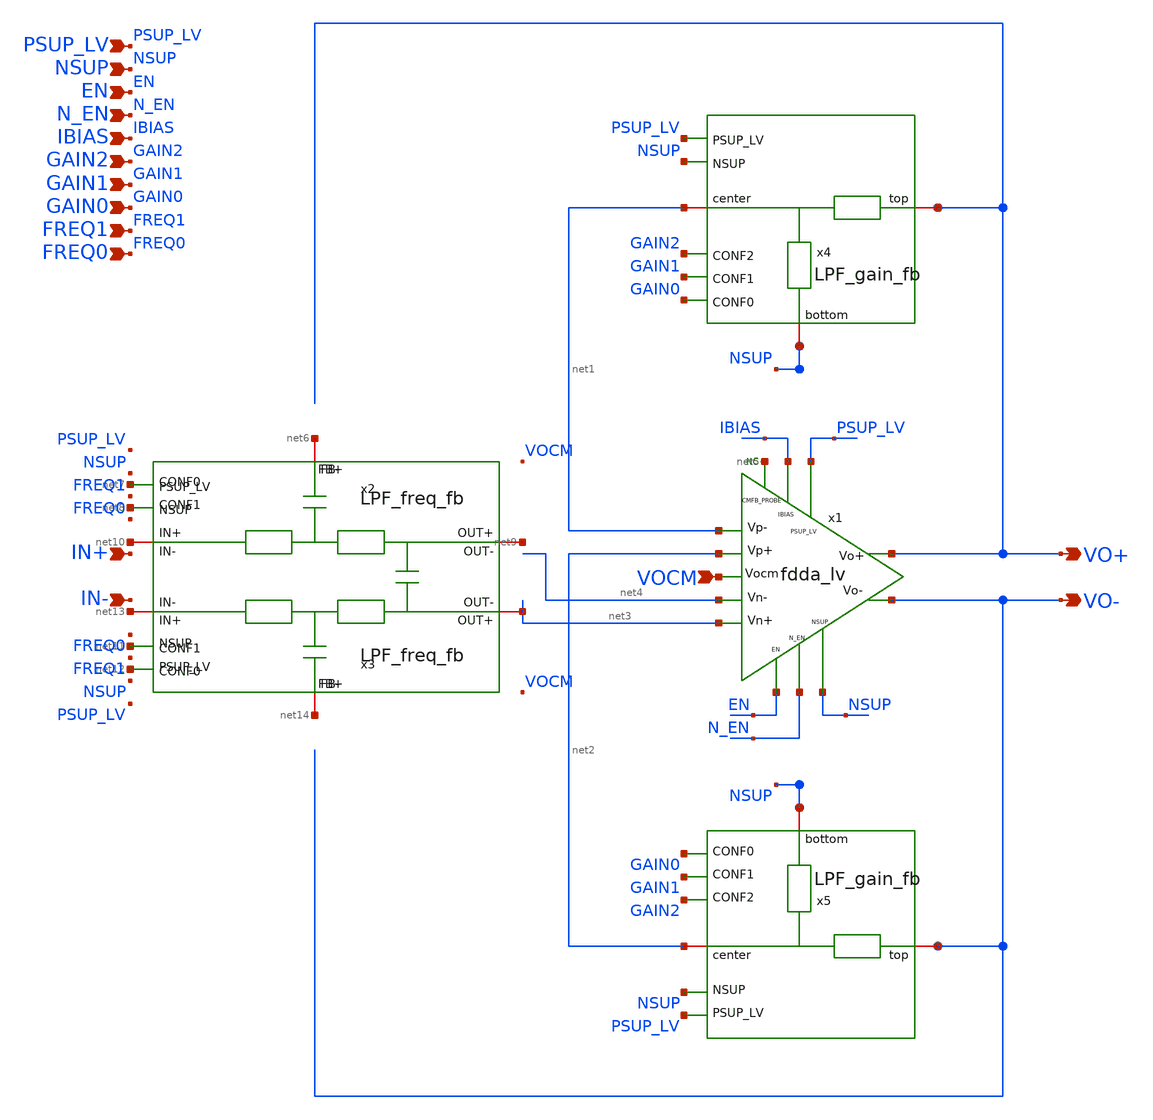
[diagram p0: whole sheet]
** sch_path: xschem/blocks/LPF/LPF.sch
**.subckt LPF NSUP EN N_EN IBIAS PSUP_LV GAIN2 VO+ VO- GAIN1 GAIN0 FREQ1 FREQ0 IN+ IN- VOCM
*.ipin NSUP
*.ipin EN
*.ipin N_EN
*.ipin IBIAS
*.ipin PSUP_LV
*.ipin GAIN2
*.opin VO+
*.opin VO-
*.ipin GAIN1
*.ipin GAIN0
*.ipin FREQ1
*.ipin FREQ0
*.ipin IN+
*.ipin IN-
*.ipin VOCM
* noconn #net5
x1 PSUP_LV net1 net4 net3 net2 VO+ VO- IBIAS N_EN EN NSUP net5 VOCM fdda_lv
x2 net6 net7 net8 net9 net10 net11 net12 net3 net13 net14 LPF_freq_fb
x3 net14 net12 net11 net3 net13 net8 net7 net9 net10 net6 LPF_freq_fb
x4 VO+ net1 PSUP_LV NSUP GAIN2 GAIN1 GAIN0 NSUP LPF_gain_fb
x5 VO- net2 PSUP_LV NSUP GAIN2 GAIN1 GAIN0 NSUP LPF_gain_fb
**.ends
.end
